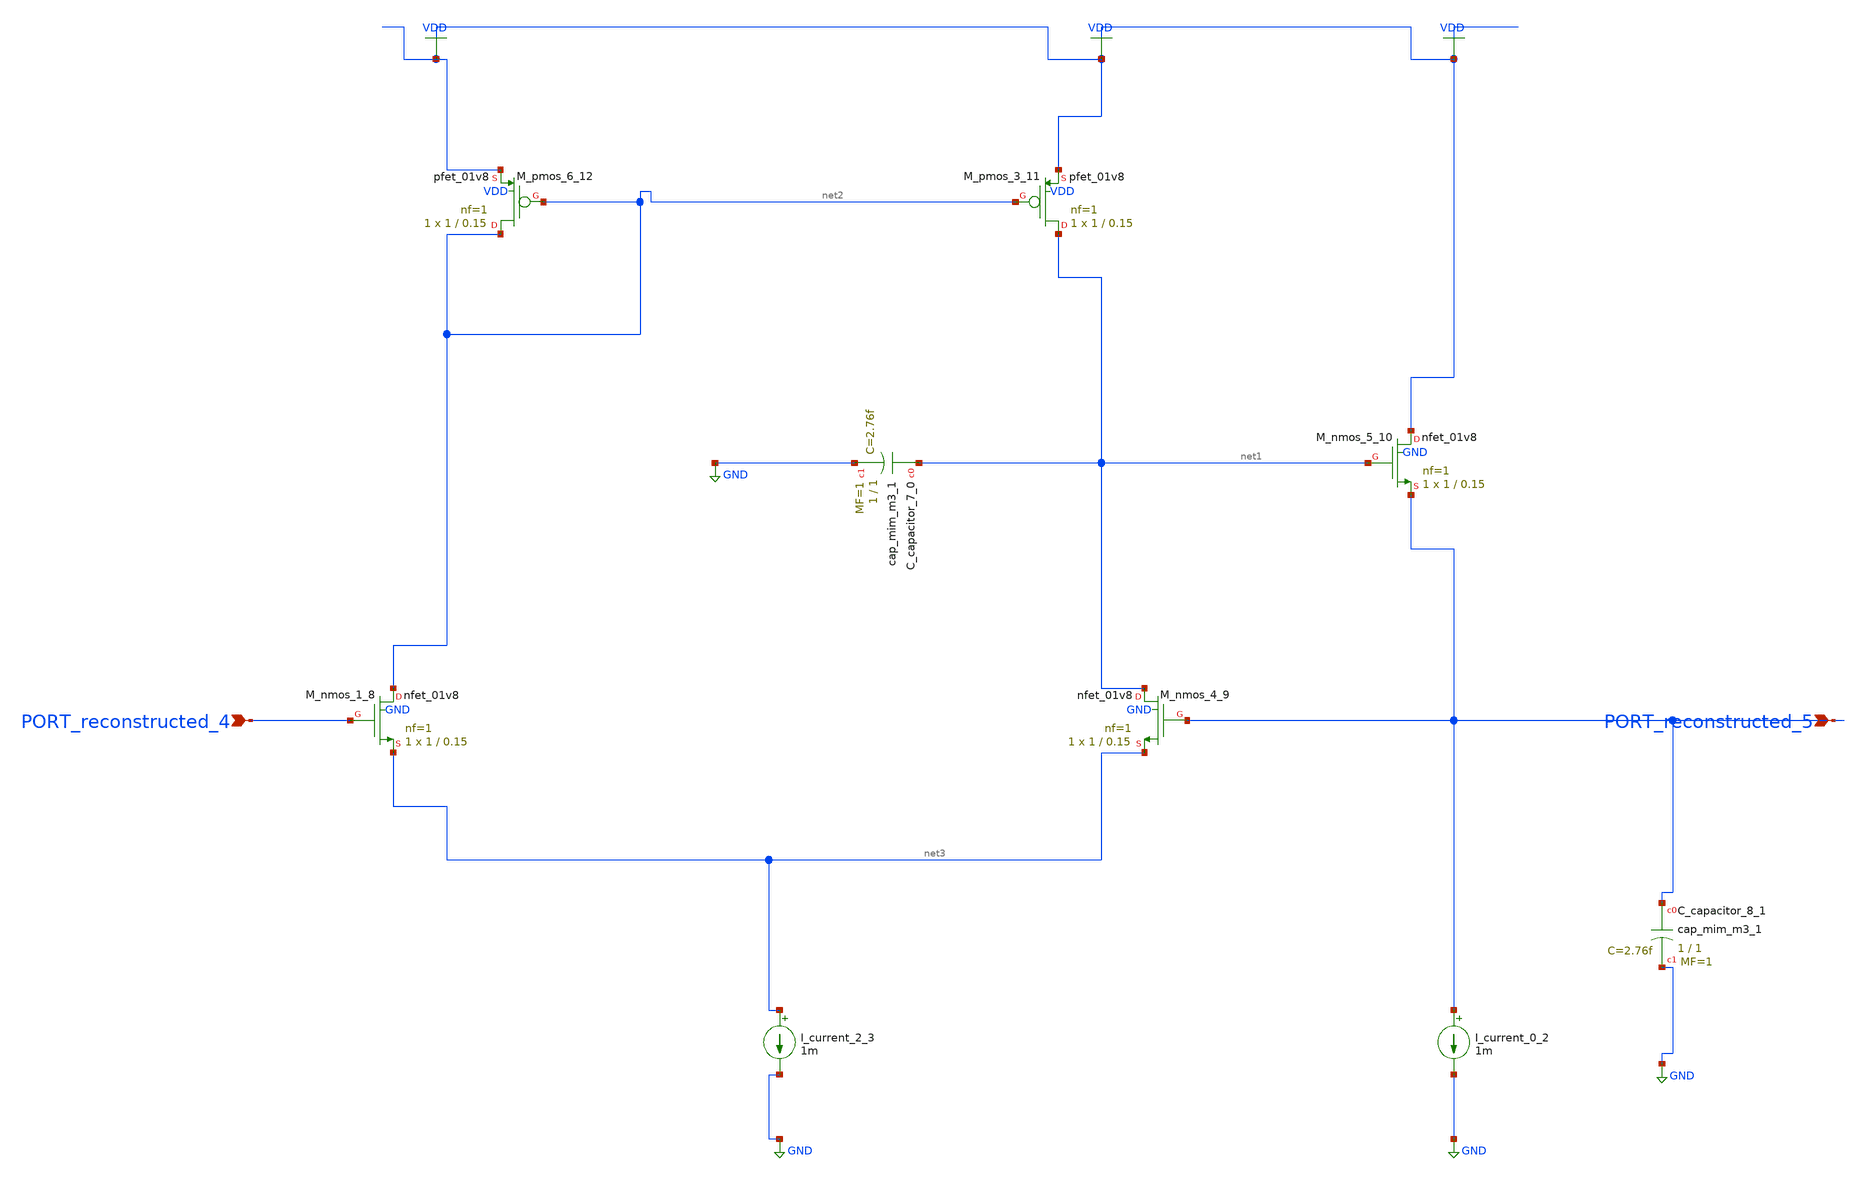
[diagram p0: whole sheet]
** sch_path: schematics/AMSNet/718.sch
**.subckt 718 PORT_reconstructed_5 PORT_reconstructed_4
*.ipin PORT_reconstructed_5
*.ipin PORT_reconstructed_4
XC_capacitor_7_0 net1 GND sky130_fd_pr__cap_mim_m3_1 W=1 L=1 MF=1 m=1
XC_capacitor_8_1 PORT_reconstructed_5 GND sky130_fd_pr__cap_mim_m3_1 W=1 L=1 MF=1 m=1
I_current_0_2 PORT_reconstructed_5 GND 1m
I_current_2_3 net3 GND 1m
XM_nmos_1_8 net2 PORT_reconstructed_4 net3 GND sky130_fd_pr__nfet_01v8 L=0.15 W=1 nf=1 ad='int((1 + 1)/2) * 1 / 1 * 0.29'
+ as='int((1 + 2)/2) * 1 / 1 * 0.29' pd='2*int((1 + 1)/2) * (1 / 1 + 0.29)' ps='2*int((1 + 2)/2) * (1 / 1 + 0.29)'
+ nrd='0.29 / 1 ' nrs='0.29 / 1 ' sa=0 sb=0 sd=0 mult=1 m=1
XM_nmos_4_9 net1 PORT_reconstructed_5 net3 GND sky130_fd_pr__nfet_01v8 L=0.15 W=1 nf=1 ad='int((1 + 1)/2) * 1 / 1 * 0.29'
+ as='int((1 + 2)/2) * 1 / 1 * 0.29' pd='2*int((1 + 1)/2) * (1 / 1 + 0.29)' ps='2*int((1 + 2)/2) * (1 / 1 + 0.29)'
+ nrd='0.29 / 1 ' nrs='0.29 / 1 ' sa=0 sb=0 sd=0 mult=1 m=1
XM_nmos_5_10 VDD net1 PORT_reconstructed_5 GND sky130_fd_pr__nfet_01v8 L=0.15 W=1 nf=1 ad='int((1 + 1)/2) * 1 / 1 * 0.29'
+ as='int((1 + 2)/2) * 1 / 1 * 0.29' pd='2*int((1 + 1)/2) * (1 / 1 + 0.29)' ps='2*int((1 + 2)/2) * (1 / 1 + 0.29)'
+ nrd='0.29 / 1 ' nrs='0.29 / 1 ' sa=0 sb=0 sd=0 mult=1 m=1
XM_pmos_3_11 net1 net2 VDD VDD sky130_fd_pr__pfet_01v8 L=0.15 W=1 nf=1 ad='int((1 + 1)/2) * 1 / 1 * 0.29'
+ as='int((1 + 2)/2) * 1 / 1 * 0.29' pd='2*int((1 + 1)/2) * (1 / 1 + 0.29)' ps='2*int((1 + 2)/2) * (1 / 1 + 0.29)'
+ nrd='0.29 / 1 ' nrs='0.29 / 1 ' sa=0 sb=0 sd=0 mult=1 m=1
XM_pmos_6_12 net2 net2 VDD VDD sky130_fd_pr__pfet_01v8 L=0.15 W=1 nf=1 ad='int((1 + 1)/2) * 1 / 1 * 0.29'
+ as='int((1 + 2)/2) * 1 / 1 * 0.29' pd='2*int((1 + 1)/2) * (1 / 1 + 0.29)' ps='2*int((1 + 2)/2) * (1 / 1 + 0.29)'
+ nrd='0.29 / 1 ' nrs='0.29 / 1 ' sa=0 sb=0 sd=0 mult=1 m=1
**.ends
.GLOBAL GND
.GLOBAL VDD
.end
